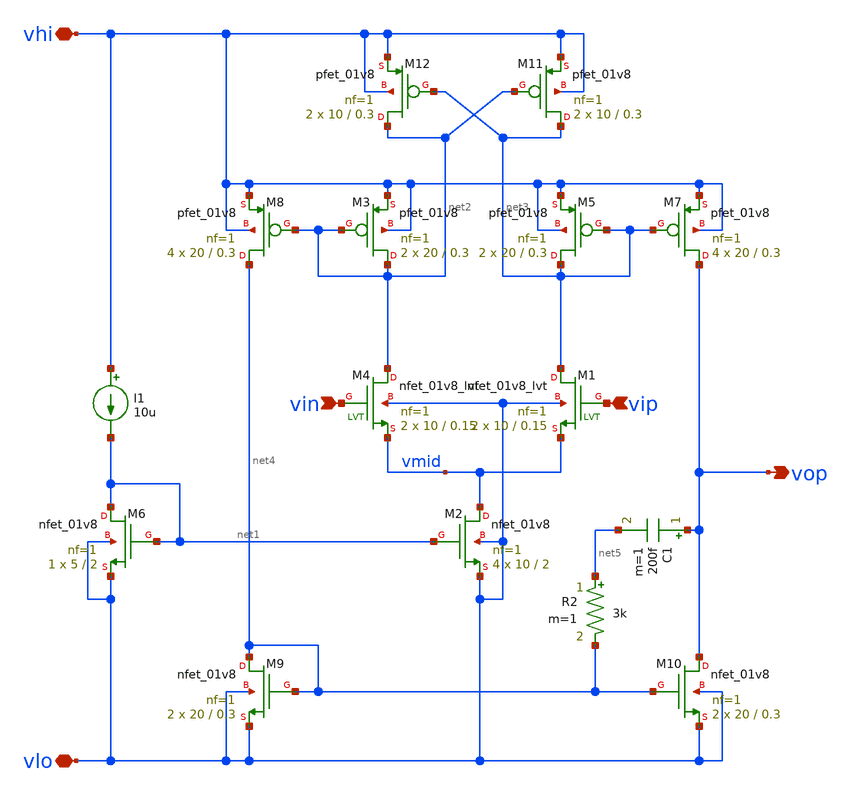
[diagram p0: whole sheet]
** sch_path: xschem/i_type_ota_model_reduced_power.sch
**.subckt i_type_ota_model_reduced_power vip vin vop vhi vlo
*.ipin vip
*.ipin vin
*.opin vop
*.iopin vhi
*.iopin vlo
XM2 vmid net1 vlo vlo sky130_fd_pr__nfet_01v8 L=2 W=10 nf=1 ad='int((nf+1)/2) * W/nf * 0.29' as='int((nf+2)/2) * W/nf * 0.29'
+ pd='2*int((nf+1)/2) * (W/nf + 0.29)' ps='2*int((nf+2)/2) * (W/nf + 0.29)' nrd='0.29 / W' nrs='0.29 / W'
+ sa=0 sb=0 sd=0 mult=4 m=4
XM6 net1 net1 vlo vlo sky130_fd_pr__nfet_01v8 L=2 W=5 nf=1 ad='int((nf+1)/2) * W/nf * 0.29' as='int((nf+2)/2) * W/nf * 0.29'
+ pd='2*int((nf+1)/2) * (W/nf + 0.29)' ps='2*int((nf+2)/2) * (W/nf + 0.29)' nrd='0.29 / W' nrs='0.29 / W'
+ sa=0 sb=0 sd=0 mult=1 m=1
I1 vhi net1 10u
XM4 net2 vin vmid vlo sky130_fd_pr__nfet_01v8_lvt L=0.15 W=10 nf=1 ad='int((nf+1)/2) * W/nf * 0.29' as='int((nf+2)/2) * W/nf * 0.29'
+ pd='2*int((nf+1)/2) * (W/nf + 0.29)' ps='2*int((nf+2)/2) * (W/nf + 0.29)' nrd='0.29 / W' nrs='0.29 / W'
+ sa=0 sb=0 sd=0 mult=2 m=2
XM1 net3 vip vmid vlo sky130_fd_pr__nfet_01v8_lvt L=0.15 W=10 nf=1 ad='int((nf+1)/2) * W/nf * 0.29' as='int((nf+2)/2) * W/nf * 0.29'
+ pd='2*int((nf+1)/2) * (W/nf + 0.29)' ps='2*int((nf+2)/2) * (W/nf + 0.29)' nrd='0.29 / W' nrs='0.29 / W'
+ sa=0 sb=0 sd=0 mult=2 m=2
XM3 net2 net2 vhi vhi sky130_fd_pr__pfet_01v8 L=0.3 W=20 nf=1 ad='int((nf+1)/2) * W/nf * 0.29' as='int((nf+2)/2) * W/nf * 0.29'
+ pd='2*int((nf+1)/2) * (W/nf + 0.29)' ps='2*int((nf+2)/2) * (W/nf + 0.29)' nrd='0.29 / W' nrs='0.29 / W'
+ sa=0 sb=0 sd=0 mult=2 m=2
XM5 net3 net3 vhi vhi sky130_fd_pr__pfet_01v8 L=0.3 W=20 nf=1 ad='int((nf+1)/2) * W/nf * 0.29' as='int((nf+2)/2) * W/nf * 0.29'
+ pd='2*int((nf+1)/2) * (W/nf + 0.29)' ps='2*int((nf+2)/2) * (W/nf + 0.29)' nrd='0.29 / W' nrs='0.29 / W'
+ sa=0 sb=0 sd=0 mult=2 m=2
XM7 vop net3 vhi vhi sky130_fd_pr__pfet_01v8 L=0.3 W=20 nf=1 ad='int((nf+1)/2) * W/nf * 0.29' as='int((nf+2)/2) * W/nf * 0.29'
+ pd='2*int((nf+1)/2) * (W/nf + 0.29)' ps='2*int((nf+2)/2) * (W/nf + 0.29)' nrd='0.29 / W' nrs='0.29 / W'
+ sa=0 sb=0 sd=0 mult=4 m=4
XM8 net4 net2 vhi vhi sky130_fd_pr__pfet_01v8 L=0.3 W=20 nf=1 ad='int((nf+1)/2) * W/nf * 0.29' as='int((nf+2)/2) * W/nf * 0.29'
+ pd='2*int((nf+1)/2) * (W/nf + 0.29)' ps='2*int((nf+2)/2) * (W/nf + 0.29)' nrd='0.29 / W' nrs='0.29 / W'
+ sa=0 sb=0 sd=0 mult=4 m=4
XM9 net4 net4 vlo vlo sky130_fd_pr__nfet_01v8 L=0.3 W=20 nf=1 ad='int((nf+1)/2) * W/nf * 0.29' as='int((nf+2)/2) * W/nf * 0.29'
+ pd='2*int((nf+1)/2) * (W/nf + 0.29)' ps='2*int((nf+2)/2) * (W/nf + 0.29)' nrd='0.29 / W' nrs='0.29 / W'
+ sa=0 sb=0 sd=0 mult=2 m=2
XM10 vop net4 vlo vlo sky130_fd_pr__nfet_01v8 L=0.3 W=20 nf=1 ad='int((nf+1)/2) * W/nf * 0.29' as='int((nf+2)/2) * W/nf * 0.29'
+ pd='2*int((nf+1)/2) * (W/nf + 0.29)' ps='2*int((nf+2)/2) * (W/nf + 0.29)' nrd='0.29 / W' nrs='0.29 / W'
+ sa=0 sb=0 sd=0 mult=2 m=2
XM11 net3 net2 vhi vhi sky130_fd_pr__pfet_01v8 L=0.3 W=10 nf=1 ad='int((nf+1)/2) * W/nf * 0.29' as='int((nf+2)/2) * W/nf * 0.29'
+ pd='2*int((nf+1)/2) * (W/nf + 0.29)' ps='2*int((nf+2)/2) * (W/nf + 0.29)' nrd='0.29 / W' nrs='0.29 / W'
+ sa=0 sb=0 sd=0 mult=2 m=2
XM12 net2 net3 vhi vhi sky130_fd_pr__pfet_01v8 L=0.3 W=10 nf=1 ad='int((nf+1)/2) * W/nf * 0.29' as='int((nf+2)/2) * W/nf * 0.29'
+ pd='2*int((nf+1)/2) * (W/nf + 0.29)' ps='2*int((nf+2)/2) * (W/nf + 0.29)' nrd='0.29 / W' nrs='0.29 / W'
+ sa=0 sb=0 sd=0 mult=2 m=2
C1 vop net5 200f m=1
R2 net5 net4 3k m=1
**.ends
.end
